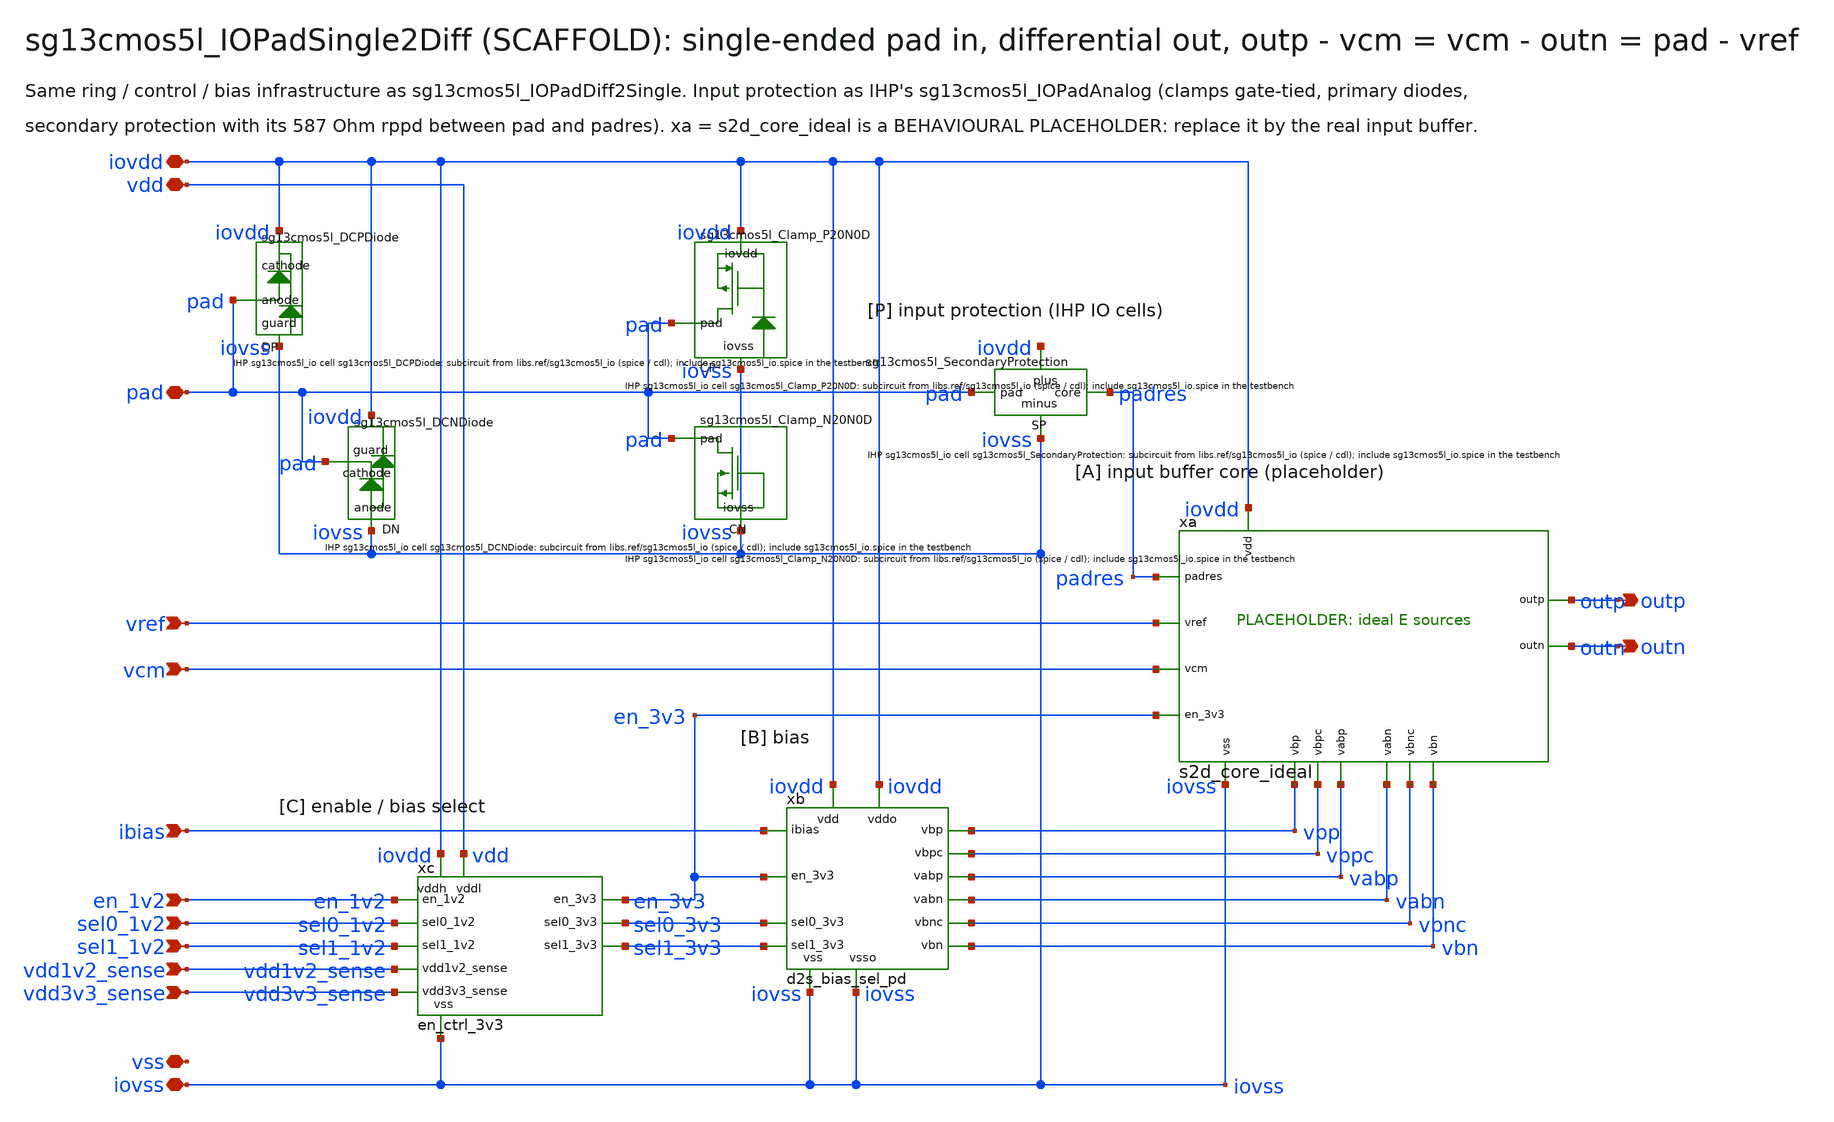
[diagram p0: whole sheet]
** sch_path: sudelbuecher/design_considerations/consolidation/enable_rework_2026-10-25/before/macros/sg13cmos5l_IOPadSingle2Diff/schematic/xschem/sg13cmos5l_IOPadSingle2Diff.sch
**.subckt sg13cmos5l_IOPadSingle2Diff iovdd iovss vdd vss pad outp outn vcm vref ibias en_1v2
*+ sel0_1v2 sel1_1v2 vdd1v2_sense vdd3v3_sense
*.iopin iovdd
*.iopin iovss
*.iopin vdd
*.iopin vss
*.iopin pad
*.opin outp
*.opin outn
*.ipin vcm
*.ipin vref
*.ipin ibias
*.ipin en_1v2
*.ipin sel0_1v2
*.ipin sel1_1v2
*.ipin vdd1v2_sense
*.ipin vdd3v3_sense
xc iovdd vdd iovss en_1v2 sel0_1v2 sel1_1v2 vdd1v2_sense vdd3v3_sense en_3v3 sel0_3v3 sel1_3v3
+ en_ctrl_3v3
xb iovdd iovss iovdd iovss ibias vbp vbn vbpc vbnc vabp vabn en_3v3 sel0_3v3 sel1_3v3
+ d2s_bias_sel_pd
xa iovdd iovss padres vref vcm outp outn vbp vbn vbpc vbnc vabp vabn en_3v3 s2d_core_ideal
XCP iovdd iovss pad sg13cmos5l_Clamp_P20N0D
XCN iovss pad sg13cmos5l_Clamp_N20N0D
XDN iovss pad iovdd sg13cmos5l_DCNDiode
XDP pad iovdd iovss sg13cmos5l_DCPDiode
XSP padres iovss pad iovdd sg13cmos5l_SecondaryProtection
**.ends
.end
